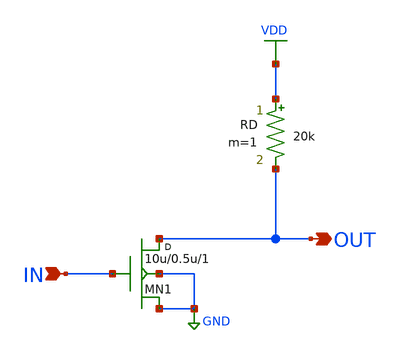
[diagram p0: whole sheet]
** sch_path: E3_238_Analog_VLSI_Circuits/11_Amplifier_Frequency_Response/cs_frequency_response.sch
**.subckt cs_frequency_response IN OUT
*.ipin IN
*.opin OUT
MN1 OUT IN GND GND nmos w=10u l=0.5u m=1
RD VDD OUT 20k m=1
**** begin user architecture code

.include /home/anirudh/Analog_VLSI_Projects/models/cmos_180nm.mod
VDD VDD 0 DC 1.8
VIN IN 0 DC 0.57 AC 1
CL OUT GND 1p

.control
  op
  ac dec 30 1 1G
  plot db(v(OUT))
  alter CL = 5p
  ac dec 30 1 1G
  plot db(v(OUT))
.endc


**** end user architecture code
**.ends
.GLOBAL VDD
.GLOBAL GND
.end
